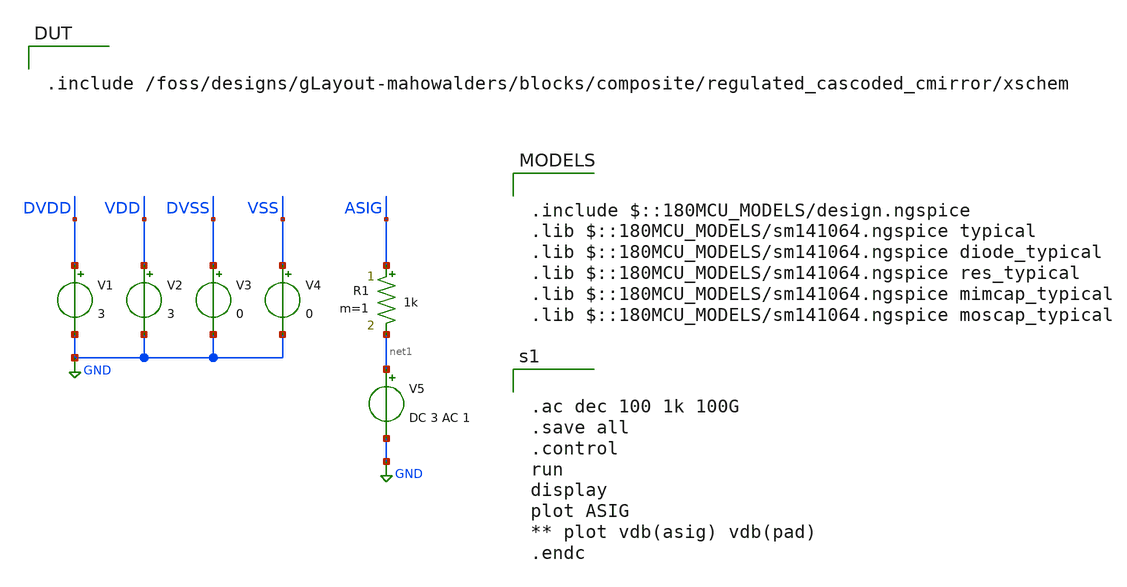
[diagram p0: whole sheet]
** sch_path: blocks/composite/regulated_cascoded_cmirror/xschem/analog_io_ac_pex.sch
**.subckt analog_io_ac_pex
V1 DVDD GND 3
V2 VDD GND 3
V3 DVSS GND 0
V4 VSS GND 0
V5 net1 GND DC 3 AC 1
R1 ASIG net1 1k m=1
**** begin user architecture code


.ac dec 100 1k 100G
.save all
.control
run
display
plot ASIG
** plot vdb(asig) vdb(pad)
.endc



.include $::180MCU_MODELS/design.ngspice
.lib $::180MCU_MODELS/sm141064.ngspice typical
.lib $::180MCU_MODELS/sm141064.ngspice diode_typical
.lib $::180MCU_MODELS/sm141064.ngspice res_typical
.lib $::180MCU_MODELS/sm141064.ngspice mimcap_typical
.lib $::180MCU_MODELS/sm141064.ngspice moscap_typical


.include /foss/designs/gLayout-mahowalders/blocks/composite/regulated_cascoded_cmirror/xschem
**** end user architecture code
**.ends
.GLOBAL GND
.end
